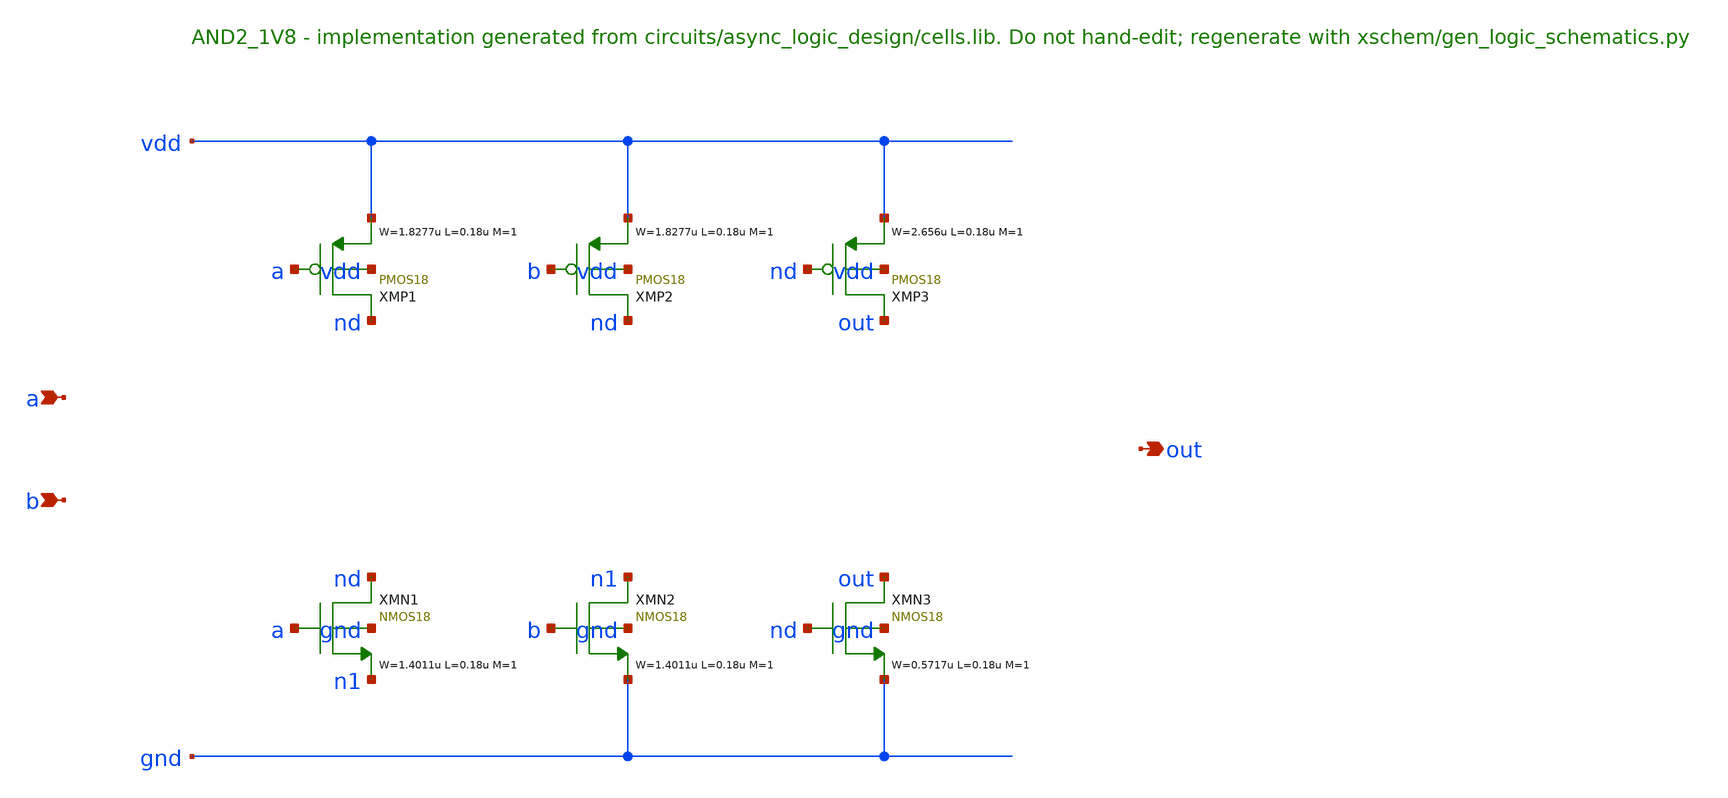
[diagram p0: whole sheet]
** sch_path: xschem/logic/AND2_1V8.sch
**.subckt AND2_1V8 a b out
*.ipin a
*.ipin b
*.opin out
XMP1 nd a vdd vdd PMOS18 W=1.8277u L=0.18u M=1 MM_SIGMA=0
XMP2 nd b vdd vdd PMOS18 W=1.8277u L=0.18u M=1 MM_SIGMA=0
XMP3 out nd vdd vdd PMOS18 W=2.656u L=0.18u M=1 MM_SIGMA=0
XMN1 nd a n1 gnd NMOS18 W=1.4011u L=0.18u M=1 MM_SIGMA=0
XMN2 n1 b gnd gnd NMOS18 W=1.4011u L=0.18u M=1 MM_SIGMA=0
XMN3 out nd gnd gnd NMOS18 W=0.5717u L=0.18u M=1 MM_SIGMA=0
**.ends
.end
